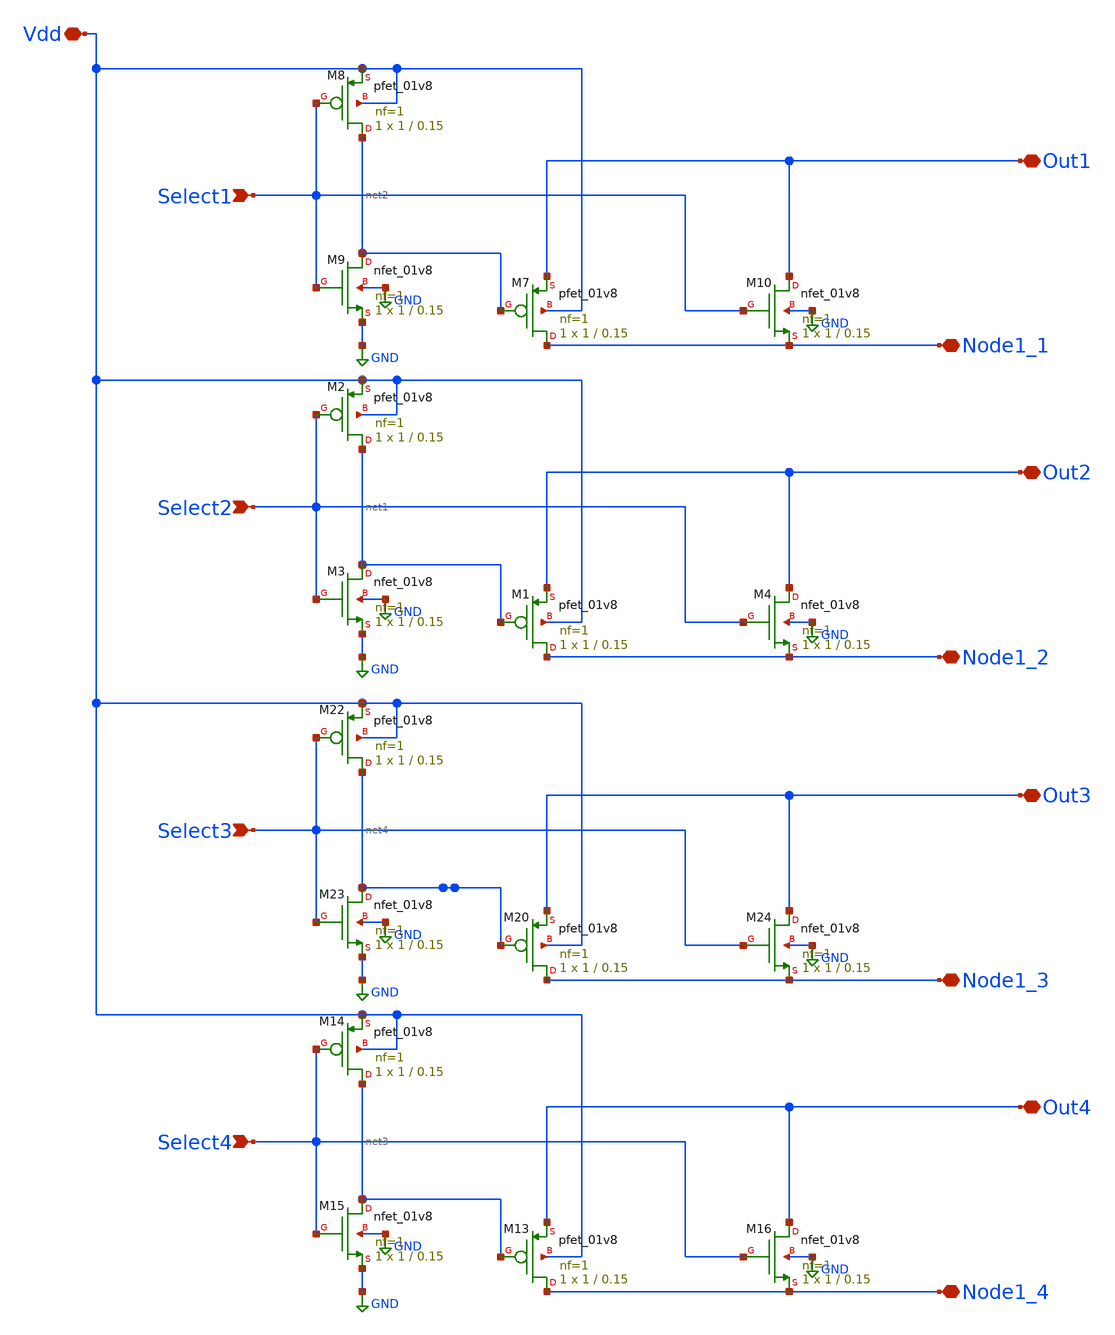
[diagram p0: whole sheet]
** sch_path: libs.ref/sky130_hilas_sc/xschem/sky130_hilas_Tgate4Single01.sch
**.subckt sky130_hilas_Tgate4Single01 Select2 Vdd Node1_2 Out2 Select1 Node1_1 Out1 Select4 Node1_4
*+ Out4 Select3 Node1_3 Out3
*.ipin Select2
*.iopin Vdd
*.iopin Node1_2
*.iopin Out2
*.ipin Select1
*.iopin Node1_1
*.iopin Out1
*.ipin Select4
*.iopin Node1_4
*.iopin Out4
*.ipin Select3
*.iopin Node1_3
*.iopin Out3
XM1 Node1_2 net1 Out2 Vdd sky130_fd_pr__pfet_01v8 L=0.15 W=1 nf=1 ad='int((nf+1)/2) * W/nf * 0.29' as='int((nf+2)/2) * W/nf * 0.29'
+ pd='2*int((nf+1)/2) * (W/nf + 0.29)' ps='2*int((nf+2)/2) * (W/nf + 0.29)' nrd='0.29 / W' nrs='0.29 / W'
+ sa=0 sb=0 sd=0 mult=1 m=1
XM2 net1 Select2 Vdd Vdd sky130_fd_pr__pfet_01v8 L=0.15 W=1 nf=1 ad='int((nf+1)/2) * W/nf * 0.29' as='int((nf+2)/2) * W/nf * 0.29'
+ pd='2*int((nf+1)/2) * (W/nf + 0.29)' ps='2*int((nf+2)/2) * (W/nf + 0.29)' nrd='0.29 / W' nrs='0.29 / W'
+ sa=0 sb=0 sd=0 mult=1 m=1
XM3 net1 Select2 GND GND sky130_fd_pr__nfet_01v8 L=0.15 W=1 nf=1 ad='int((nf+1)/2) * W/nf * 0.29' as='int((nf+2)/2) * W/nf * 0.29'
+ pd='2*int((nf+1)/2) * (W/nf + 0.29)' ps='2*int((nf+2)/2) * (W/nf + 0.29)' nrd='0.29 / W' nrs='0.29 / W'
+ sa=0 sb=0 sd=0 mult=1 m=1
XM4 Out2 Select2 Node1_2 GND sky130_fd_pr__nfet_01v8 L=0.15 W=1 nf=1 ad='int((nf+1)/2) * W/nf * 0.29'
+ as='int((nf+2)/2) * W/nf * 0.29' pd='2*int((nf+1)/2) * (W/nf + 0.29)' ps='2*int((nf+2)/2) * (W/nf + 0.29)'
+ nrd='0.29 / W' nrs='0.29 / W' sa=0 sb=0 sd=0 mult=1 m=1
XM7 Node1_1 net2 Out1 Vdd sky130_fd_pr__pfet_01v8 L=0.15 W=1 nf=1 ad='int((nf+1)/2) * W/nf * 0.29' as='int((nf+2)/2) * W/nf * 0.29'
+ pd='2*int((nf+1)/2) * (W/nf + 0.29)' ps='2*int((nf+2)/2) * (W/nf + 0.29)' nrd='0.29 / W' nrs='0.29 / W'
+ sa=0 sb=0 sd=0 mult=1 m=1
XM8 net2 Select1 Vdd Vdd sky130_fd_pr__pfet_01v8 L=0.15 W=1 nf=1 ad='int((nf+1)/2) * W/nf * 0.29' as='int((nf+2)/2) * W/nf * 0.29'
+ pd='2*int((nf+1)/2) * (W/nf + 0.29)' ps='2*int((nf+2)/2) * (W/nf + 0.29)' nrd='0.29 / W' nrs='0.29 / W'
+ sa=0 sb=0 sd=0 mult=1 m=1
XM9 net2 Select1 GND GND sky130_fd_pr__nfet_01v8 L=0.15 W=1 nf=1 ad='int((nf+1)/2) * W/nf * 0.29' as='int((nf+2)/2) * W/nf * 0.29'
+ pd='2*int((nf+1)/2) * (W/nf + 0.29)' ps='2*int((nf+2)/2) * (W/nf + 0.29)' nrd='0.29 / W' nrs='0.29 / W'
+ sa=0 sb=0 sd=0 mult=1 m=1
XM10 Out1 Select1 Node1_1 GND sky130_fd_pr__nfet_01v8 L=0.15 W=1 nf=1 ad='int((nf+1)/2) * W/nf * 0.29'
+ as='int((nf+2)/2) * W/nf * 0.29' pd='2*int((nf+1)/2) * (W/nf + 0.29)' ps='2*int((nf+2)/2) * (W/nf + 0.29)'
+ nrd='0.29 / W' nrs='0.29 / W' sa=0 sb=0 sd=0 mult=1 m=1
XM13 Node1_4 net3 Out4 Vdd sky130_fd_pr__pfet_01v8 L=0.15 W=1 nf=1 ad='int((nf+1)/2) * W/nf * 0.29' as='int((nf+2)/2) * W/nf * 0.29'
+ pd='2*int((nf+1)/2) * (W/nf + 0.29)' ps='2*int((nf+2)/2) * (W/nf + 0.29)' nrd='0.29 / W' nrs='0.29 / W'
+ sa=0 sb=0 sd=0 mult=1 m=1
XM14 net3 Select4 Vdd Vdd sky130_fd_pr__pfet_01v8 L=0.15 W=1 nf=1 ad='int((nf+1)/2) * W/nf * 0.29' as='int((nf+2)/2) * W/nf * 0.29'
+ pd='2*int((nf+1)/2) * (W/nf + 0.29)' ps='2*int((nf+2)/2) * (W/nf + 0.29)' nrd='0.29 / W' nrs='0.29 / W'
+ sa=0 sb=0 sd=0 mult=1 m=1
XM15 net3 Select4 GND GND sky130_fd_pr__nfet_01v8 L=0.15 W=1 nf=1 ad='int((nf+1)/2) * W/nf * 0.29' as='int((nf+2)/2) * W/nf * 0.29'
+ pd='2*int((nf+1)/2) * (W/nf + 0.29)' ps='2*int((nf+2)/2) * (W/nf + 0.29)' nrd='0.29 / W' nrs='0.29 / W'
+ sa=0 sb=0 sd=0 mult=1 m=1
XM16 Out4 Select4 Node1_4 GND sky130_fd_pr__nfet_01v8 L=0.15 W=1 nf=1 ad='int((nf+1)/2) * W/nf * 0.29'
+ as='int((nf+2)/2) * W/nf * 0.29' pd='2*int((nf+1)/2) * (W/nf + 0.29)' ps='2*int((nf+2)/2) * (W/nf + 0.29)'
+ nrd='0.29 / W' nrs='0.29 / W' sa=0 sb=0 sd=0 mult=1 m=1
XM20 Node1_3 net4 Out3 Vdd sky130_fd_pr__pfet_01v8 L=0.15 W=1 nf=1 ad='int((nf+1)/2) * W/nf * 0.29' as='int((nf+2)/2) * W/nf * 0.29'
+ pd='2*int((nf+1)/2) * (W/nf + 0.29)' ps='2*int((nf+2)/2) * (W/nf + 0.29)' nrd='0.29 / W' nrs='0.29 / W'
+ sa=0 sb=0 sd=0 mult=1 m=1
XM22 net4 Select3 Vdd Vdd sky130_fd_pr__pfet_01v8 L=0.15 W=1 nf=1 ad='int((nf+1)/2) * W/nf * 0.29' as='int((nf+2)/2) * W/nf * 0.29'
+ pd='2*int((nf+1)/2) * (W/nf + 0.29)' ps='2*int((nf+2)/2) * (W/nf + 0.29)' nrd='0.29 / W' nrs='0.29 / W'
+ sa=0 sb=0 sd=0 mult=1 m=1
XM23 net4 Select3 GND GND sky130_fd_pr__nfet_01v8 L=0.15 W=1 nf=1 ad='int((nf+1)/2) * W/nf * 0.29' as='int((nf+2)/2) * W/nf * 0.29'
+ pd='2*int((nf+1)/2) * (W/nf + 0.29)' ps='2*int((nf+2)/2) * (W/nf + 0.29)' nrd='0.29 / W' nrs='0.29 / W'
+ sa=0 sb=0 sd=0 mult=1 m=1
XM24 Out3 Select3 Node1_3 GND sky130_fd_pr__nfet_01v8 L=0.15 W=1 nf=1 ad='int((nf+1)/2) * W/nf * 0.29'
+ as='int((nf+2)/2) * W/nf * 0.29' pd='2*int((nf+1)/2) * (W/nf + 0.29)' ps='2*int((nf+2)/2) * (W/nf + 0.29)'
+ nrd='0.29 / W' nrs='0.29 / W' sa=0 sb=0 sd=0 mult=1 m=1
**.ends
.GLOBAL GND
.end
